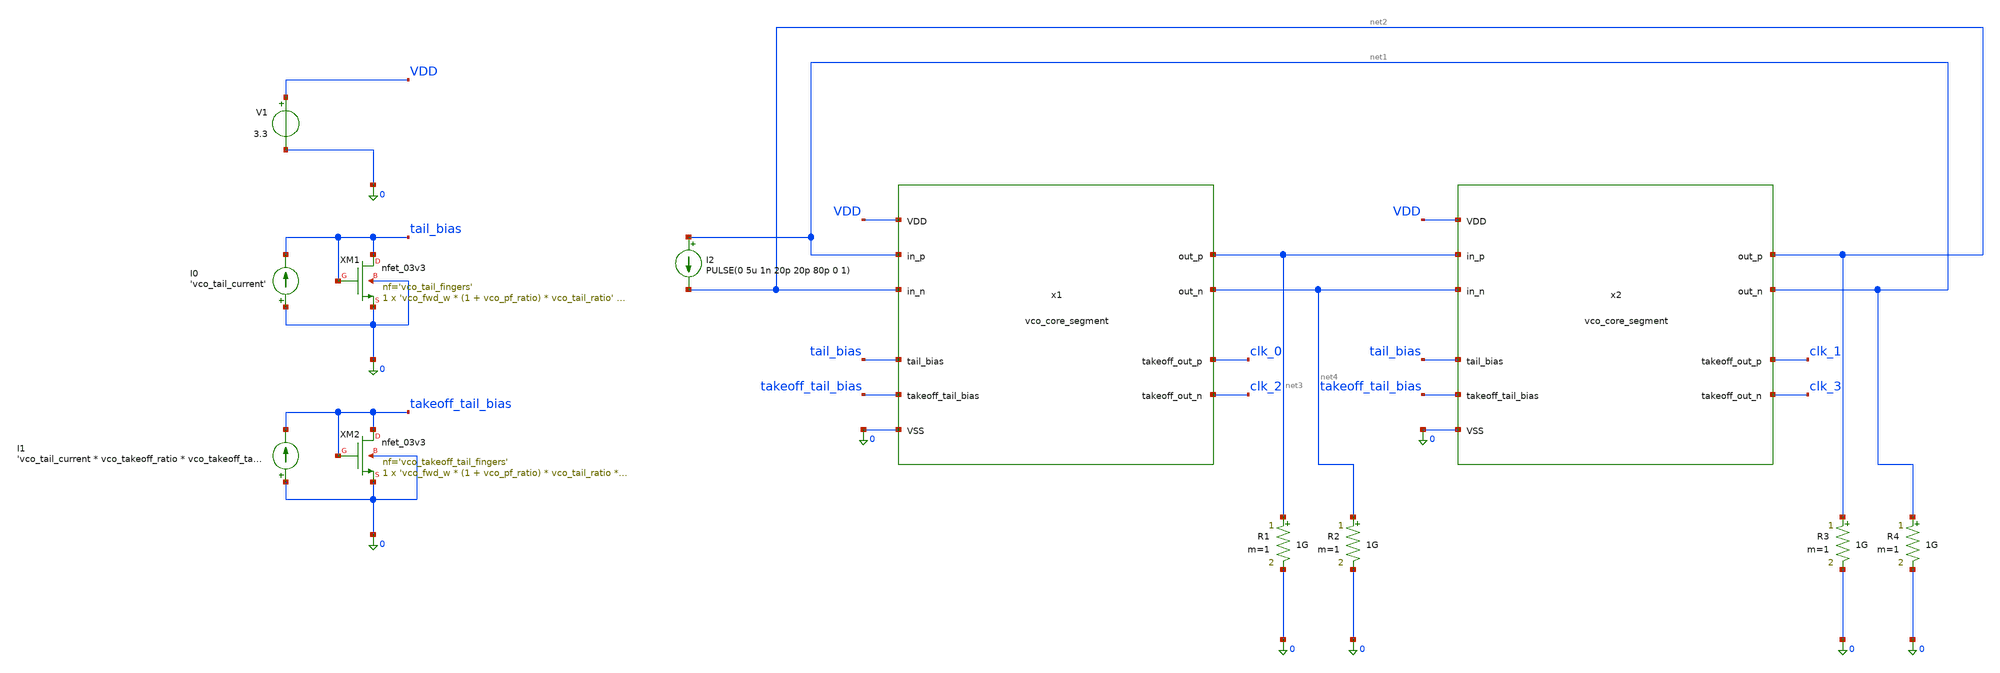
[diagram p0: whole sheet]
** sch_path: xschem/vco_core_tb.sch
**.subckt vco_core_tb
x1 0 VDD net4 net3 net1 net2 clk_2 clk_0 tail_bias takeoff_tail_bias vco_core_segment
XM1 tail_bias tail_bias 0 0 nfet_03v3 L='vco_tail_l' W='vco_fwd_w * (1 + vco_pf_ratio) * vco_tail_ratio'
+ nf='vco_tail_fingers' ad='int((nf+1)/2) * W/nf * 0.18u' as='int((nf+2)/2) * W/nf * 0.18u' pd='2*int((nf+1)/2) * (W/nf + 0.18u)'
+ ps='2*int((nf+2)/2) * (W/nf + 0.18u)' nrd='0.18u / W' nrs='0.18u / W' sa=0 sb=0 sd=0 m=1
x2 0 VDD net1 net2 net3 net4 clk_3 clk_1 tail_bias takeoff_tail_bias vco_core_segment
XM2 takeoff_tail_bias takeoff_tail_bias 0 0 nfet_03v3 L='vco_takeoff_tail_l' W='vco_fwd_w * (1 + vco_pf_ratio) * vco_tail_ratio * vco_takeoff_ratio'
+ nf='vco_takeoff_tail_fingers' ad='int((nf+1)/2) * W/nf * 0.18u' as='int((nf+2)/2) * W/nf * 0.18u' pd='2*int((nf+1)/2) * (W/nf + 0.18u)'
+ ps='2*int((nf+2)/2) * (W/nf + 0.18u)' nrd='0.18u / W' nrs='0.18u / W' sa=0 sb=0 sd=0 m=1
V1 VDD 0 3.3
I0 0 tail_bias 'vco_tail_current'
I1 0 takeoff_tail_bias 'vco_tail_current * vco_takeoff_ratio * vco_takeoff_tail_adjust'
I2 net1 net2 PULSE(0 5u 1n 20p 20p 80p 0 1)
R1 net3 0 1G m=1
R2 net4 0 1G m=1
R3 net2 0 1G m=1
R4 net1 0 1G m=1
**** begin user architecture code
 .include $::180MCU_MODELS/design.ngspice
.lib $::180MCU_MODELS/sm141064.ngspice typical
.lib $::180MCU_MODELS/sm141064.ngspice res_typical


.option savecurrents

.param vco_fwd_w=6u
.param vco_pf_S=1.5
.param vco_pf_ratio='1/vco_pf_S'
.param vco_fwd_fingers=2
.param vco_pf_fingers=1
.param vco_tail_fingers=20
.param vco_takeoff_tail_fingers=10
.param vco_takeoff_ratio=0.1
.param vco_takeoff_fingers=1
.param vco_tail_ratio=50
.param vco_tail_l=1u
.param vco_takeoff_tail_ratio=5
.param vco_takeoff_tail_l=1u
.param vco_load_w=1u
.param vco_load_r=4k
.param vco_load_l='vco_load_r/1000 * vco_load_w'
.param vco_takeoff_load_adjust=1
.param vco_takeoff_load_w=1u
.param vco_takeoff_load_r='(vco_load_r / vco_takeoff_ratio) * vco_takeoff_load_adjust'
.param vco_takeoff_load_l='vco_takeoff_load_r/1000 * vco_takeoff_load_w'
.param vco_takeoff_tail_adjust=1
.param vco_tail_current=512u

.control
save all
tran 5p 50n
plot v(clk_0) v(clk_1) v(clk_2) v(clk_3)
plot net1 net2 net3 net4 x1.net1
.endc
**** end user architecture code
**.ends

* expanding   symbol:  vco_core_segment.sym # of pins=10
** sym_path: xschem/vco_core_segment.sym
** sch_path: xschem/vco_core_segment.sch
.subckt vco_core_segment VSS VDD out_n out_p in_p in_n takeoff_out_n takeoff_out_p tail_bias
+ takeoff_tail_bias
*.ipin VSS
*.ipin VDD
*.opin out_n
*.opin out_p
*.ipin in_p
*.ipin in_n
*.opin takeoff_out_n
*.opin takeoff_out_p
*.ipin tail_bias
*.ipin takeoff_tail_bias
XM1 out_n in_p net1 VSS nfet_03v3 L=0.28u W='vco_fwd_w' nf='vco_fwd_fingers' ad='int((nf+1)/2) * W/nf * 0.18u'
+ as='int((nf+2)/2) * W/nf * 0.18u' pd='2*int((nf+1)/2) * (W/nf + 0.18u)' ps='2*int((nf+2)/2) * (W/nf + 0.18u)'
+ nrd='0.18u / W' nrs='0.18u / W' sa=0 sb=0 sd=0 m=1
XM3 out_n out_p net1 VSS nfet_03v3 L=0.28u W='vco_fwd_w * vco_pf_ratio' nf='vco_pf_fingers' ad='int((nf+1)/2) * W/nf * 0.18u'
+ as='int((nf+2)/2) * W/nf * 0.18u' pd='2*int((nf+1)/2) * (W/nf + 0.18u)' ps='2*int((nf+2)/2) * (W/nf + 0.18u)'
+ nrd='0.18u / W' nrs='0.18u / W' sa=0 sb=0 sd=0 m=1
XM4 out_p out_n net1 VSS nfet_03v3 L=0.28u W='vco_fwd_w * vco_pf_ratio' nf='vco_pf_fingers' ad='int((nf+1)/2) * W/nf * 0.18u'
+ as='int((nf+2)/2) * W/nf * 0.18u' pd='2*int((nf+1)/2) * (W/nf + 0.18u)' ps='2*int((nf+2)/2) * (W/nf + 0.18u)'
+ nrd='0.18u / W' nrs='0.18u / W' sa=0 sb=0 sd=0 m=1
XM5 net1 tail_bias VSS VSS nfet_03v3 L='vco_tail_l' W='vco_fwd_w * (1 + vco_pf_ratio) * vco_tail_ratio'
+ nf='vco_tail_fingers' ad='int((nf+1)/2) * W/nf * 0.18u' as='int((nf+2)/2) * W/nf * 0.18u' pd='2*int((nf+1)/2) * (W/nf + 0.18u)'
+ ps='2*int((nf+2)/2) * (W/nf + 0.18u)' nrd='0.18u / W' nrs='0.18u / W' sa=0 sb=0 sd=0 m=1
XM2 out_p in_n net1 VSS nfet_03v3 L=0.28u W='vco_fwd_w' nf='vco_fwd_fingers' ad='int((nf+1)/2) * W/nf * 0.18u'
+ as='int((nf+2)/2) * W/nf * 0.18u' pd='2*int((nf+1)/2) * (W/nf + 0.18u)' ps='2*int((nf+2)/2) * (W/nf + 0.18u)'
+ nrd='0.18u / W' nrs='0.18u / W' sa=0 sb=0 sd=0 m=1
XR1 out_n VDD VSS ppolyf_u_1k r_width='vco_load_w' r_length='vco_load_l' m=1
XR2 out_p VDD VSS ppolyf_u_1k r_width='vco_load_w' r_length='vco_load_l' m=1
XM6 takeoff_out_n out_p net2 VSS nfet_03v3 L=0.28u W='vco_fwd_w' nf='vco_fwd_fingers' ad='int((nf+1)/2) * W/nf * 0.18u'
+ as='int((nf+2)/2) * W/nf * 0.18u' pd='2*int((nf+1)/2) * (W/nf + 0.18u)' ps='2*int((nf+2)/2) * (W/nf + 0.18u)'
+ nrd='0.18u / W' nrs='0.18u / W' sa=0 sb=0 sd=0 m=1
XM7 takeoff_out_p out_n net2 VSS nfet_03v3 L=0.28u W='vco_fwd_w' nf='vco_fwd_fingers' ad='int((nf+1)/2) * W/nf * 0.18u'
+ as='int((nf+2)/2) * W/nf * 0.18u' pd='2*int((nf+1)/2) * (W/nf + 0.18u)' ps='2*int((nf+2)/2) * (W/nf + 0.18u)'
+ nrd='0.18u / W' nrs='0.18u / W' sa=0 sb=0 sd=0 m=1
XM8 net2 takeoff_tail_bias VSS VSS nfet_03v3 L='vco_takeoff_tail_l' W='vco_fwd_w * (1 + vco_pf_ratio) * vco_tail_ratio * vco_takeoff_ratio'
+ nf='vco_takeoff_tail_fingers' ad='int((nf+1)/2) * W/nf * 0.18u' as='int((nf+2)/2) * W/nf * 0.18u' pd='2*int((nf+1)/2) * (W/nf + 0.18u)'
+ ps='2*int((nf+2)/2) * (W/nf + 0.18u)' nrd='0.18u / W' nrs='0.18u / W' sa=0 sb=0 sd=0 m=1
XR3 takeoff_out_n VDD VSS ppolyf_u_1k r_width='vco_takeoff_load_w' r_length='vco_takeoff_load_l' m=1
XR4 takeoff_out_p VDD VSS ppolyf_u_1k r_width='vco_takeoff_load_w' r_length='vco_takeoff_load_l' m=1
.ends

.end
